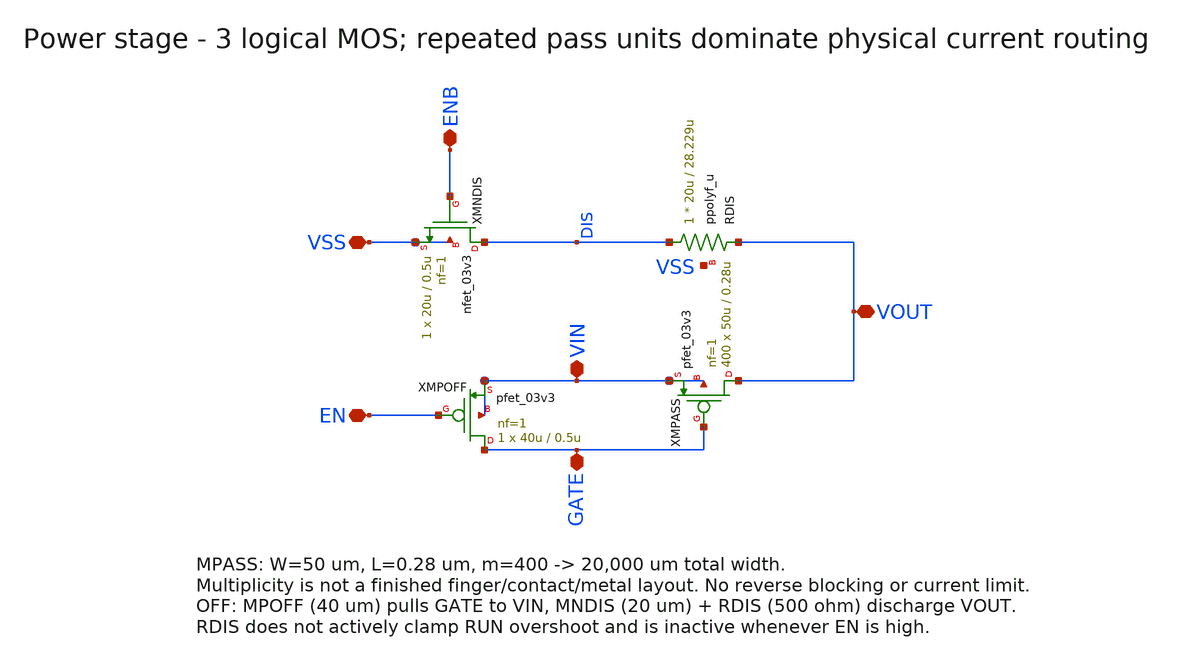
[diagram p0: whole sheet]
** sch_path: schematics/ldo_power_stage.sch
**.subckt ldo_power_stage VIN VSS EN ENB GATE VOUT
*.iopin VIN
*.iopin VSS
*.iopin EN
*.iopin ENB
*.iopin GATE
*.iopin VOUT
XMPASS VOUT GATE VIN VIN pfet_03v3 L=0.28u W=50u nf=1 ad='int((nf+1)/2)*W/nf*0.18u' as='int((nf+2)/2)*W/nf*0.18u'
+ pd='2*int((nf+1)/2)*(W/nf+0.18u)' ps='2*int((nf+2)/2)*(W/nf+0.18u)' nrd='0.18u/W' nrs='0.18u/W' sa=0
+ sb=0 sd=0 m=400 par=400
XMPOFF GATE EN VIN VIN pfet_03v3 L=0.5u W=40u nf=1 ad='int((nf+1)/2)*W/nf*0.18u' as='int((nf+2)/2)*W/nf*0.18u'
+ pd='2*int((nf+1)/2)*(W/nf+0.18u)' ps='2*int((nf+2)/2)*(W/nf+0.18u)' nrd='0.18u/W' nrs='0.18u/W' sa=0
+ sb=0 sd=0 m=1 par=1
XRDIS DIS VOUT VSS ppolyf_u r_width=20u r_length=28.229u m=1
XMNDIS DIS ENB VSS VSS nfet_03v3 L=0.5u W=20u nf=1 ad='int((nf+1)/2)*W/nf*0.18u' as='int((nf+2)/2)*W/nf*0.18u'
+ pd='2*int((nf+1)/2)*(W/nf+0.18u)' ps='2*int((nf+2)/2)*(W/nf+0.18u)' nrd='0.18u/W' nrs='0.18u/W' sa=0
+ sb=0 sd=0 m=1 par=1
**.ends
.end
